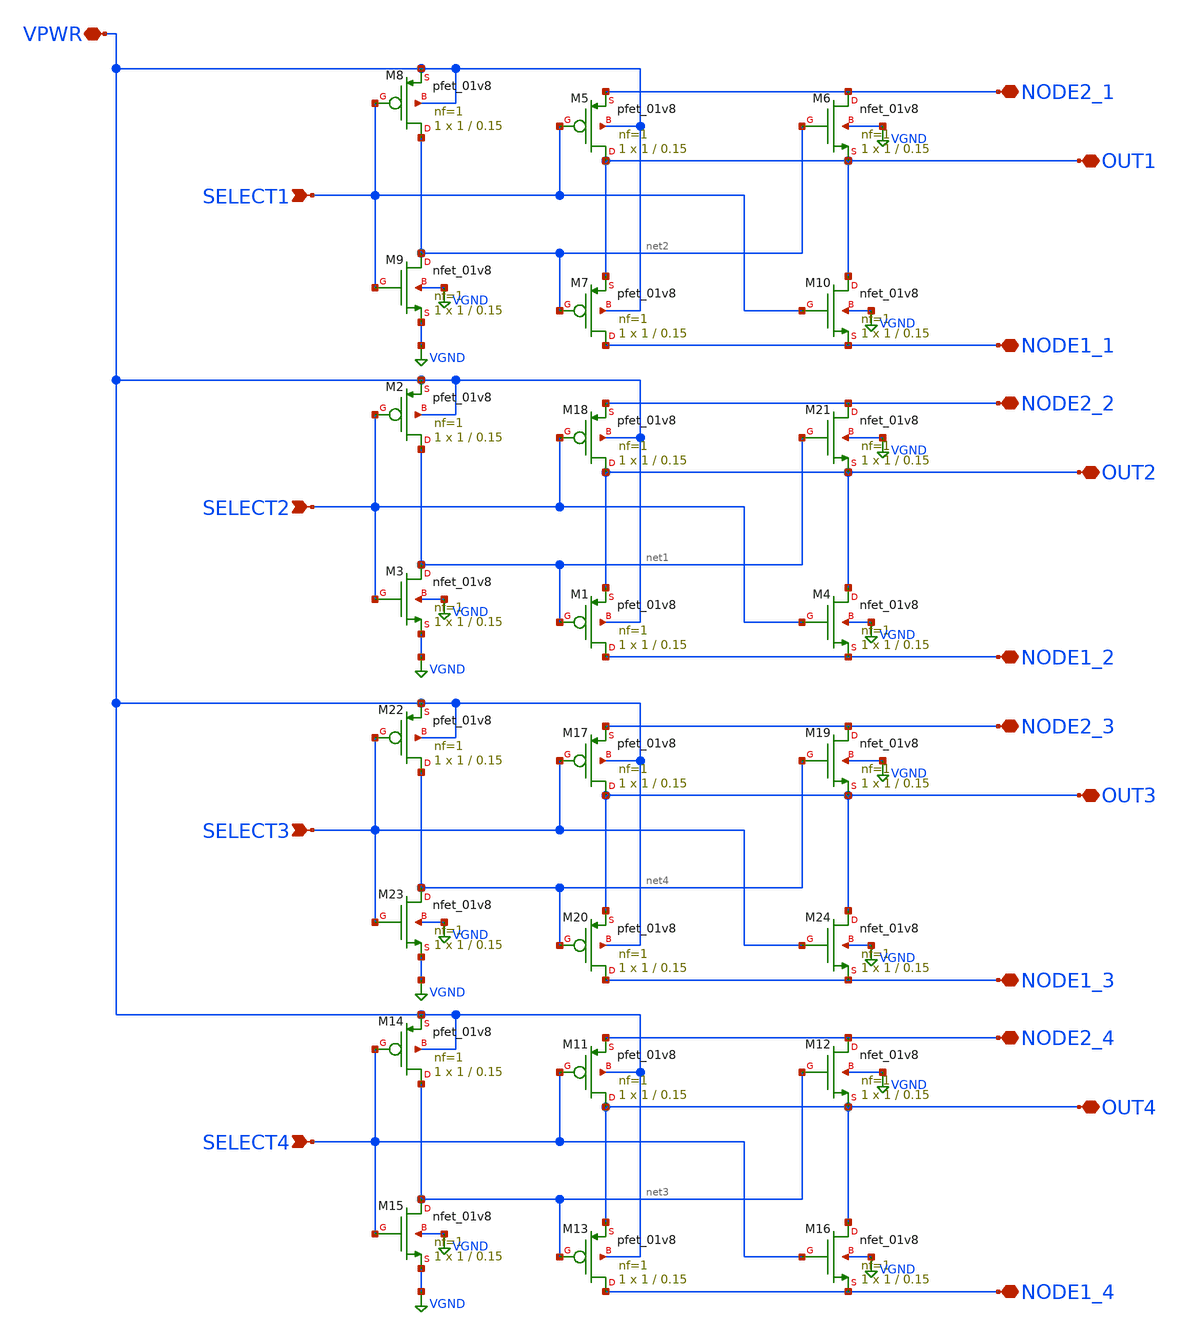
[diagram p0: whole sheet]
** sch_path: libs.ref/sky130_hilas_sc/xschem/sky130_hilas_Tgate4Double01.sch
**.subckt sky130_hilas_Tgate4Double01 SELECT2 VPWR NODE1_2 OUT2 NODE2_2 SELECT1 NODE1_1 OUT1 NODE2_1
*+ SELECT4 NODE1_4 OUT4 NODE2_4 SELECT3 NODE1_3 OUT3 NODE2_3
*.ipin SELECT2
*.iopin VPWR
*.iopin NODE1_2
*.iopin OUT2
*.iopin NODE2_2
*.ipin SELECT1
*.iopin NODE1_1
*.iopin OUT1
*.iopin NODE2_1
*.ipin SELECT4
*.iopin NODE1_4
*.iopin OUT4
*.iopin NODE2_4
*.ipin SELECT3
*.iopin NODE1_3
*.iopin OUT3
*.iopin NODE2_3
XM18 OUT2 SELECT2 NODE2_2 VPWR sky130_fd_pr__pfet_01v8 L=0.15 W=1 nf=1 ad='int((nf+1)/2) * W/nf * 0.29'
+ as='int((nf+2)/2) * W/nf * 0.29' pd='2*int((nf+1)/2) * (W/nf + 0.29)' ps='2*int((nf+2)/2) * (W/nf + 0.29)'
+ nrd='0.29 / W' nrs='0.29 / W' sa=0 sb=0 sd=0 mult=1 m=1
XM21 NODE2_2 net1 OUT2 VGND sky130_fd_pr__nfet_01v8 L=0.15 W=1 nf=1 ad='int((nf+1)/2) * W/nf * 0.29'
+ as='int((nf+2)/2) * W/nf * 0.29' pd='2*int((nf+1)/2) * (W/nf + 0.29)' ps='2*int((nf+2)/2) * (W/nf + 0.29)'
+ nrd='0.29 / W' nrs='0.29 / W' sa=0 sb=0 sd=0 mult=1 m=1
XM1 NODE1_2 net1 OUT2 VPWR sky130_fd_pr__pfet_01v8 L=0.15 W=1 nf=1 ad='int((nf+1)/2) * W/nf * 0.29' as='int((nf+2)/2) * W/nf * 0.29'
+ pd='2*int((nf+1)/2) * (W/nf + 0.29)' ps='2*int((nf+2)/2) * (W/nf + 0.29)' nrd='0.29 / W' nrs='0.29 / W'
+ sa=0 sb=0 sd=0 mult=1 m=1
XM2 net1 SELECT2 VPWR VPWR sky130_fd_pr__pfet_01v8 L=0.15 W=1 nf=1 ad='int((nf+1)/2) * W/nf * 0.29' as='int((nf+2)/2) * W/nf * 0.29'
+ pd='2*int((nf+1)/2) * (W/nf + 0.29)' ps='2*int((nf+2)/2) * (W/nf + 0.29)' nrd='0.29 / W' nrs='0.29 / W'
+ sa=0 sb=0 sd=0 mult=1 m=1
XM3 net1 SELECT2 VGND VGND sky130_fd_pr__nfet_01v8 L=0.15 W=1 nf=1 ad='int((nf+1)/2) * W/nf * 0.29' as='int((nf+2)/2) * W/nf * 0.29'
+ pd='2*int((nf+1)/2) * (W/nf + 0.29)' ps='2*int((nf+2)/2) * (W/nf + 0.29)' nrd='0.29 / W' nrs='0.29 / W'
+ sa=0 sb=0 sd=0 mult=1 m=1
XM4 OUT2 SELECT2 NODE1_2 VGND sky130_fd_pr__nfet_01v8 L=0.15 W=1 nf=1 ad='int((nf+1)/2) * W/nf * 0.29'
+ as='int((nf+2)/2) * W/nf * 0.29' pd='2*int((nf+1)/2) * (W/nf + 0.29)' ps='2*int((nf+2)/2) * (W/nf + 0.29)'
+ nrd='0.29 / W' nrs='0.29 / W' sa=0 sb=0 sd=0 mult=1 m=1
XM5 OUT1 SELECT1 NODE2_1 VPWR sky130_fd_pr__pfet_01v8 L=0.15 W=1 nf=1 ad='int((nf+1)/2) * W/nf * 0.29'
+ as='int((nf+2)/2) * W/nf * 0.29' pd='2*int((nf+1)/2) * (W/nf + 0.29)' ps='2*int((nf+2)/2) * (W/nf + 0.29)'
+ nrd='0.29 / W' nrs='0.29 / W' sa=0 sb=0 sd=0 mult=1 m=1
XM6 NODE2_1 net2 OUT1 VGND sky130_fd_pr__nfet_01v8 L=0.15 W=1 nf=1 ad='int((nf+1)/2) * W/nf * 0.29' as='int((nf+2)/2) * W/nf * 0.29'
+ pd='2*int((nf+1)/2) * (W/nf + 0.29)' ps='2*int((nf+2)/2) * (W/nf + 0.29)' nrd='0.29 / W' nrs='0.29 / W'
+ sa=0 sb=0 sd=0 mult=1 m=1
XM7 NODE1_1 net2 OUT1 VPWR sky130_fd_pr__pfet_01v8 L=0.15 W=1 nf=1 ad='int((nf+1)/2) * W/nf * 0.29' as='int((nf+2)/2) * W/nf * 0.29'
+ pd='2*int((nf+1)/2) * (W/nf + 0.29)' ps='2*int((nf+2)/2) * (W/nf + 0.29)' nrd='0.29 / W' nrs='0.29 / W'
+ sa=0 sb=0 sd=0 mult=1 m=1
XM8 net2 SELECT1 VPWR VPWR sky130_fd_pr__pfet_01v8 L=0.15 W=1 nf=1 ad='int((nf+1)/2) * W/nf * 0.29' as='int((nf+2)/2) * W/nf * 0.29'
+ pd='2*int((nf+1)/2) * (W/nf + 0.29)' ps='2*int((nf+2)/2) * (W/nf + 0.29)' nrd='0.29 / W' nrs='0.29 / W'
+ sa=0 sb=0 sd=0 mult=1 m=1
XM9 net2 SELECT1 VGND VGND sky130_fd_pr__nfet_01v8 L=0.15 W=1 nf=1 ad='int((nf+1)/2) * W/nf * 0.29' as='int((nf+2)/2) * W/nf * 0.29'
+ pd='2*int((nf+1)/2) * (W/nf + 0.29)' ps='2*int((nf+2)/2) * (W/nf + 0.29)' nrd='0.29 / W' nrs='0.29 / W'
+ sa=0 sb=0 sd=0 mult=1 m=1
XM10 OUT1 SELECT1 NODE1_1 VGND sky130_fd_pr__nfet_01v8 L=0.15 W=1 nf=1 ad='int((nf+1)/2) * W/nf * 0.29'
+ as='int((nf+2)/2) * W/nf * 0.29' pd='2*int((nf+1)/2) * (W/nf + 0.29)' ps='2*int((nf+2)/2) * (W/nf + 0.29)'
+ nrd='0.29 / W' nrs='0.29 / W' sa=0 sb=0 sd=0 mult=1 m=1
XM11 OUT4 SELECT4 NODE2_4 VPWR sky130_fd_pr__pfet_01v8 L=0.15 W=1 nf=1 ad='int((nf+1)/2) * W/nf * 0.29'
+ as='int((nf+2)/2) * W/nf * 0.29' pd='2*int((nf+1)/2) * (W/nf + 0.29)' ps='2*int((nf+2)/2) * (W/nf + 0.29)'
+ nrd='0.29 / W' nrs='0.29 / W' sa=0 sb=0 sd=0 mult=1 m=1
XM12 NODE2_4 net3 OUT4 VGND sky130_fd_pr__nfet_01v8 L=0.15 W=1 nf=1 ad='int((nf+1)/2) * W/nf * 0.29'
+ as='int((nf+2)/2) * W/nf * 0.29' pd='2*int((nf+1)/2) * (W/nf + 0.29)' ps='2*int((nf+2)/2) * (W/nf + 0.29)'
+ nrd='0.29 / W' nrs='0.29 / W' sa=0 sb=0 sd=0 mult=1 m=1
XM13 NODE1_4 net3 OUT4 VPWR sky130_fd_pr__pfet_01v8 L=0.15 W=1 nf=1 ad='int((nf+1)/2) * W/nf * 0.29'
+ as='int((nf+2)/2) * W/nf * 0.29' pd='2*int((nf+1)/2) * (W/nf + 0.29)' ps='2*int((nf+2)/2) * (W/nf + 0.29)'
+ nrd='0.29 / W' nrs='0.29 / W' sa=0 sb=0 sd=0 mult=1 m=1
XM14 net3 SELECT4 VPWR VPWR sky130_fd_pr__pfet_01v8 L=0.15 W=1 nf=1 ad='int((nf+1)/2) * W/nf * 0.29'
+ as='int((nf+2)/2) * W/nf * 0.29' pd='2*int((nf+1)/2) * (W/nf + 0.29)' ps='2*int((nf+2)/2) * (W/nf + 0.29)'
+ nrd='0.29 / W' nrs='0.29 / W' sa=0 sb=0 sd=0 mult=1 m=1
XM15 net3 SELECT4 VGND VGND sky130_fd_pr__nfet_01v8 L=0.15 W=1 nf=1 ad='int((nf+1)/2) * W/nf * 0.29'
+ as='int((nf+2)/2) * W/nf * 0.29' pd='2*int((nf+1)/2) * (W/nf + 0.29)' ps='2*int((nf+2)/2) * (W/nf + 0.29)'
+ nrd='0.29 / W' nrs='0.29 / W' sa=0 sb=0 sd=0 mult=1 m=1
XM16 OUT4 SELECT4 NODE1_4 VGND sky130_fd_pr__nfet_01v8 L=0.15 W=1 nf=1 ad='int((nf+1)/2) * W/nf * 0.29'
+ as='int((nf+2)/2) * W/nf * 0.29' pd='2*int((nf+1)/2) * (W/nf + 0.29)' ps='2*int((nf+2)/2) * (W/nf + 0.29)'
+ nrd='0.29 / W' nrs='0.29 / W' sa=0 sb=0 sd=0 mult=1 m=1
XM17 OUT3 SELECT3 NODE2_3 VPWR sky130_fd_pr__pfet_01v8 L=0.15 W=1 nf=1 ad='int((nf+1)/2) * W/nf * 0.29'
+ as='int((nf+2)/2) * W/nf * 0.29' pd='2*int((nf+1)/2) * (W/nf + 0.29)' ps='2*int((nf+2)/2) * (W/nf + 0.29)'
+ nrd='0.29 / W' nrs='0.29 / W' sa=0 sb=0 sd=0 mult=1 m=1
XM19 NODE2_3 net4 OUT3 VGND sky130_fd_pr__nfet_01v8 L=0.15 W=1 nf=1 ad='int((nf+1)/2) * W/nf * 0.29'
+ as='int((nf+2)/2) * W/nf * 0.29' pd='2*int((nf+1)/2) * (W/nf + 0.29)' ps='2*int((nf+2)/2) * (W/nf + 0.29)'
+ nrd='0.29 / W' nrs='0.29 / W' sa=0 sb=0 sd=0 mult=1 m=1
XM20 NODE1_3 net4 OUT3 VPWR sky130_fd_pr__pfet_01v8 L=0.15 W=1 nf=1 ad='int((nf+1)/2) * W/nf * 0.29'
+ as='int((nf+2)/2) * W/nf * 0.29' pd='2*int((nf+1)/2) * (W/nf + 0.29)' ps='2*int((nf+2)/2) * (W/nf + 0.29)'
+ nrd='0.29 / W' nrs='0.29 / W' sa=0 sb=0 sd=0 mult=1 m=1
XM22 net4 SELECT3 VPWR VPWR sky130_fd_pr__pfet_01v8 L=0.15 W=1 nf=1 ad='int((nf+1)/2) * W/nf * 0.29'
+ as='int((nf+2)/2) * W/nf * 0.29' pd='2*int((nf+1)/2) * (W/nf + 0.29)' ps='2*int((nf+2)/2) * (W/nf + 0.29)'
+ nrd='0.29 / W' nrs='0.29 / W' sa=0 sb=0 sd=0 mult=1 m=1
XM23 net4 SELECT3 VGND VGND sky130_fd_pr__nfet_01v8 L=0.15 W=1 nf=1 ad='int((nf+1)/2) * W/nf * 0.29'
+ as='int((nf+2)/2) * W/nf * 0.29' pd='2*int((nf+1)/2) * (W/nf + 0.29)' ps='2*int((nf+2)/2) * (W/nf + 0.29)'
+ nrd='0.29 / W' nrs='0.29 / W' sa=0 sb=0 sd=0 mult=1 m=1
XM24 OUT3 SELECT3 NODE1_3 VGND sky130_fd_pr__nfet_01v8 L=0.15 W=1 nf=1 ad='int((nf+1)/2) * W/nf * 0.29'
+ as='int((nf+2)/2) * W/nf * 0.29' pd='2*int((nf+1)/2) * (W/nf + 0.29)' ps='2*int((nf+2)/2) * (W/nf + 0.29)'
+ nrd='0.29 / W' nrs='0.29 / W' sa=0 sb=0 sd=0 mult=1 m=1
**.ends
.GLOBAL VGND
.end
